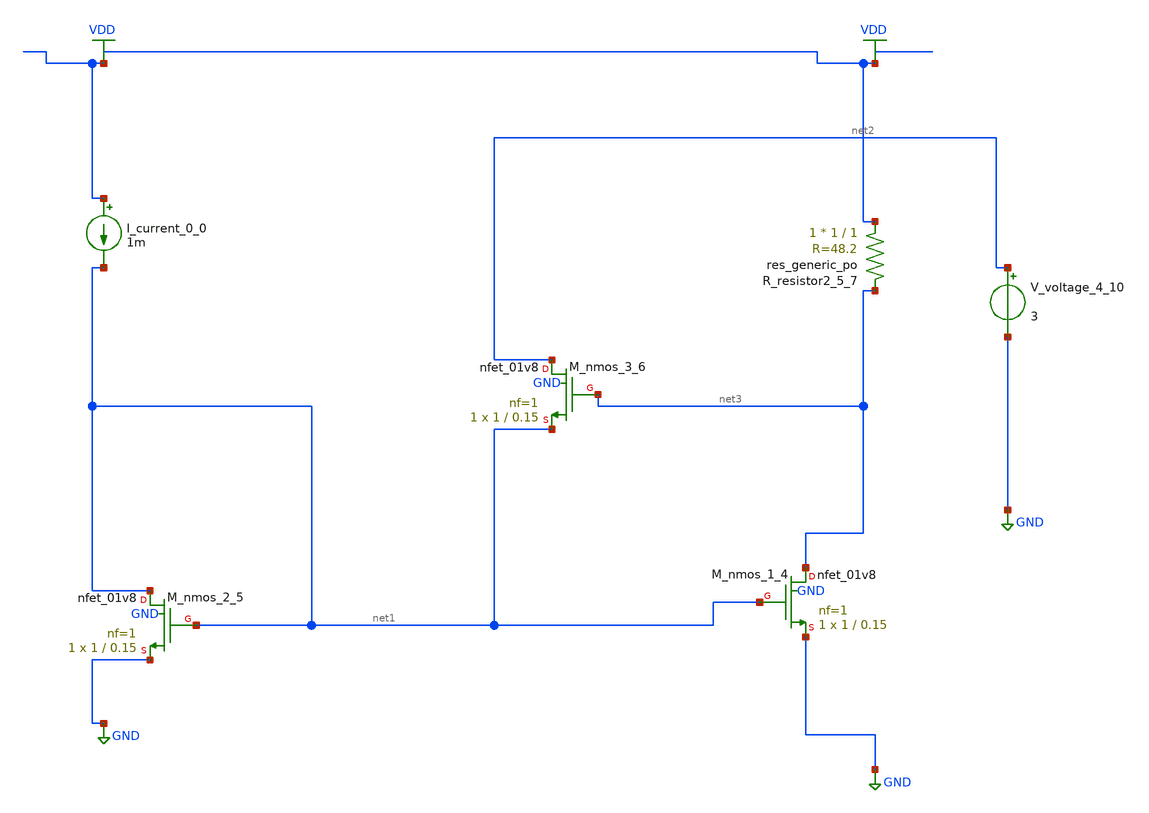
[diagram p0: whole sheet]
** sch_path: schematics/AMSNet/332.sch
**.subckt 332
I_current_0_0 VDD net1 1m
XM_nmos_1_4 net3 net1 GND GND sky130_fd_pr__nfet_01v8 L=0.15 W=1 nf=1 ad='int((1 + 1)/2) * 1 / 1 * 0.29'
+ as='int((1 + 2)/2) * 1 / 1 * 0.29' pd='2*int((1 + 1)/2) * (1 / 1 + 0.29)' ps='2*int((1 + 2)/2) * (1 / 1 + 0.29)'
+ nrd='0.29 / 1 ' nrs='0.29 / 1 ' sa=0 sb=0 sd=0 mult=1 m=1
XM_nmos_2_5 net1 net1 GND GND sky130_fd_pr__nfet_01v8 L=0.15 W=1 nf=1 ad='int((1 + 1)/2) * 1 / 1 * 0.29'
+ as='int((1 + 2)/2) * 1 / 1 * 0.29' pd='2*int((1 + 1)/2) * (1 / 1 + 0.29)' ps='2*int((1 + 2)/2) * (1 / 1 + 0.29)'
+ nrd='0.29 / 1 ' nrs='0.29 / 1 ' sa=0 sb=0 sd=0 mult=1 m=1
XM_nmos_3_6 net2 net3 net1 GND sky130_fd_pr__nfet_01v8 L=0.15 W=1 nf=1 ad='int((1 + 1)/2) * 1 / 1 * 0.29'
+ as='int((1 + 2)/2) * 1 / 1 * 0.29' pd='2*int((1 + 1)/2) * (1 / 1 + 0.29)' ps='2*int((1 + 2)/2) * (1 / 1 + 0.29)'
+ nrd='0.29 / 1 ' nrs='0.29 / 1 ' sa=0 sb=0 sd=0 mult=1 m=1
XR_resistor2_5_7 VDD net3 sky130_fd_pr__res_generic_po W=1 L=1 m=1
V_voltage_4_10 net2 GND 3
**.ends
.GLOBAL GND
.GLOBAL VDD
.end
